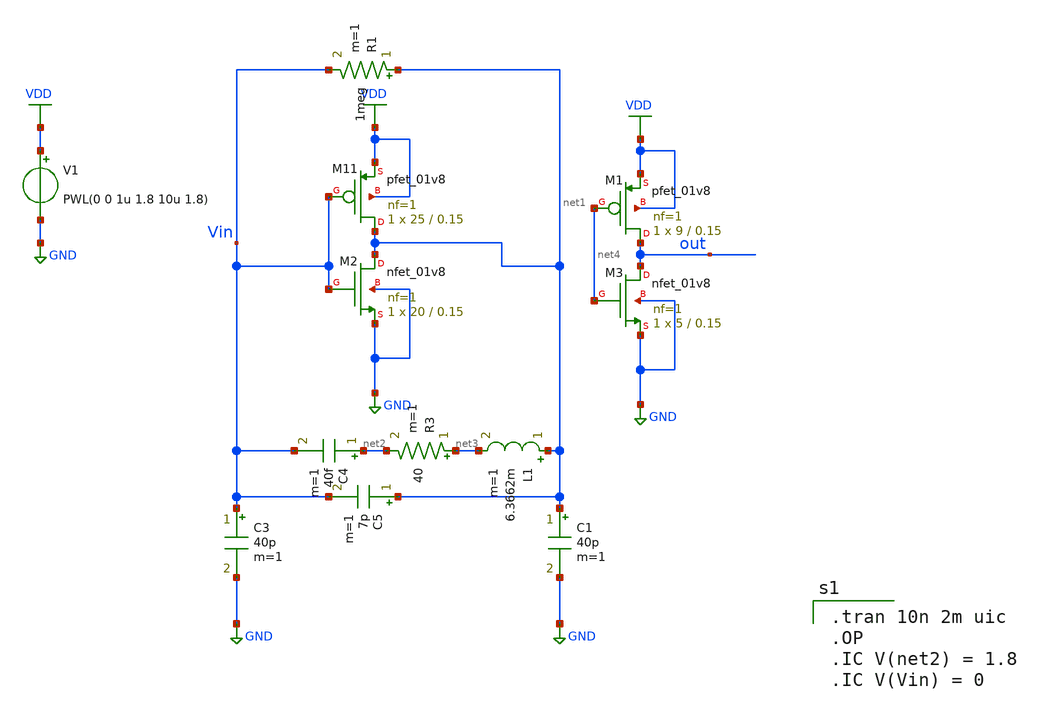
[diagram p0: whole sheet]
** sch_path: pll/xctl_lib_V2/xctl/xschem/Crystal.sch
**.subckt Crystal
C1 net1 GND 40p m=1
C3 Vin GND 40p m=1
V1 VDD GND PWL(0 0 1u 1.8 10u 1.8)
L1 net1 net3 6.3662m m=1
R3 net3 net2 40 m=1
C4 net2 Vin 40f m=1
C5 net1 Vin 7p m=1
XM11 net1 Vin VDD VDD sky130_fd_pr__pfet_01v8 L=0.15 W=25 nf=1 ad='int((nf+1)/2) * W/nf * 0.29' as='int((nf+2)/2) * W/nf * 0.29'
+ pd='2*int((nf+1)/2) * (W/nf + 0.29)' ps='2*int((nf+2)/2) * (W/nf + 0.29)' nrd='0.29 / W' nrs='0.29 / W'
+ sa=0 sb=0 sd=0 mult=1 m=1
XM2 net1 Vin GND GND sky130_fd_pr__nfet_01v8 L=0.15 W=20 nf=1 ad='int((1 + 1)/2) * 20 / 1 * 0.29' as='int((1 + 2)/2) * 20 / 1 * 0.29'
+ pd='2*int((1 + 1)/2) * (20 / 1 + 0.29)' ps='2*int((1 + 2)/2) * (20 / 1 + 0.29)' nrd='0.29 / 20 ' nrs='0.29 / 20 '
+ sa=0 sb=0 sd=0 mult=1 m=1
XM1 out net4 VDD VDD sky130_fd_pr__pfet_01v8 L=0.15 W=9 nf=1 ad='int((nf+1)/2) * W/nf * 0.29' as='int((nf+2)/2) * W/nf * 0.29'
+ pd='2*int((nf+1)/2) * (W/nf + 0.29)' ps='2*int((nf+2)/2) * (W/nf + 0.29)' nrd='0.29 / W' nrs='0.29 / W'
+ sa=0 sb=0 sd=0 mult=1 m=1
XM3 out net4 GND GND sky130_fd_pr__nfet_01v8 L=0.15 W=5 nf=1 ad='int((1 + 1)/2) * 5 / 1 * 0.29' as='int((1 + 2)/2) * 5 / 1 * 0.29'
+ pd='2*int((1 + 1)/2) * (5 / 1 + 0.29)' ps='2*int((1 + 2)/2) * (5 / 1 + 0.29)' nrd='0.29 / 5 ' nrs='0.29 / 5 '
+ sa=0 sb=0 sd=0 mult=1 m=1
R1 net1 Vin 1meg m=1
**** begin user architecture code

** opencircuitdesign pdks install
.lib $::SKYWATER_MODELS/sky130.lib.spice tt



.tran 10n 2m uic
.OP
.IC V(net2) = 1.8
.IC V(Vin) = 0


**** end user architecture code
**.ends
.GLOBAL GND
.GLOBAL VDD
.end
